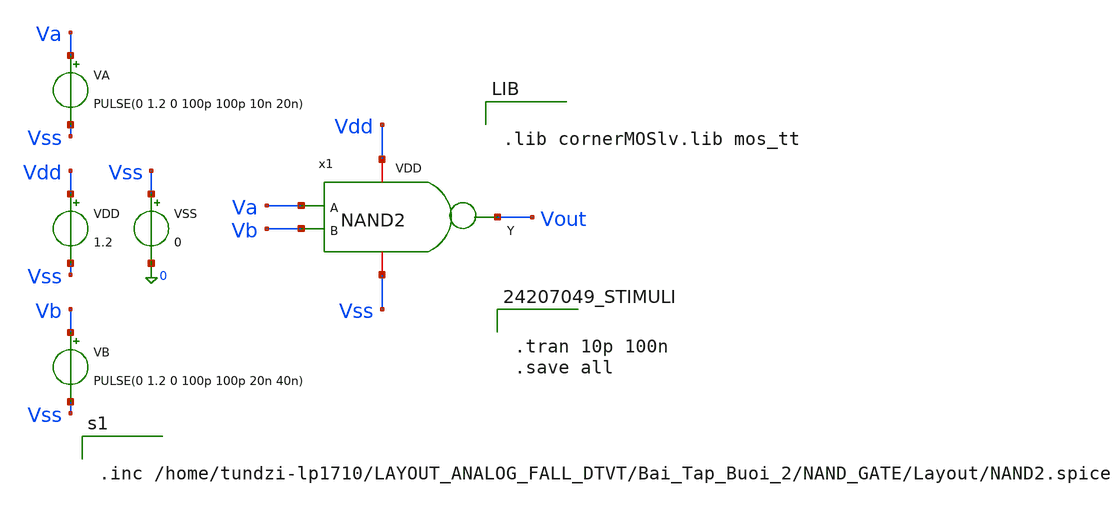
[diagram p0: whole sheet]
** sch_path: logic_gate/NAND2/Layout_Post-Simulation/NAND2_tb.sch
**.subckt NAND2_tb
VA Va Vss PULSE(0 1.2 0 100p 100p 10n 20n)
VB Vb Vss PULSE(0 1.2 0 100p 100p 20n 40n)
VDD Vdd Vss 1.2
VSS Vss 0 0
x1 Vb Va Vout Vdd Vss NAND2
**** begin user architecture code


.lib cornerMOSlv.lib mos_tt




.tran 10p 100n
.save all




.inc /home/tundzi-lp1710/LAYOUT_ANALOG_FALL_DTVT/Bai_Tap_Buoi_2/NAND_GATE/Layout/NAND2.spice


**** end user architecture code
**.ends
.end
